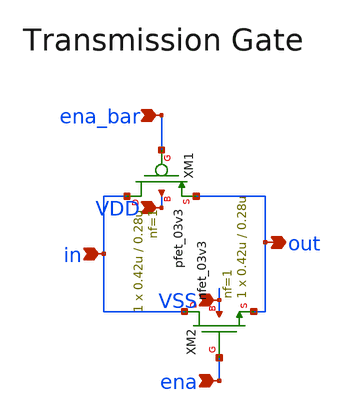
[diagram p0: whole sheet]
** sch_path: designs/libs/core_digital/schem/transmission_gate.sch
**.subckt transmission_gate in ena_bar ena VSS VDD out
*.ipin in
*.ipin ena_bar
*.ipin ena
*.ipin VSS
*.ipin VDD
*.opin out
XM1 in ena_bar out VDD pfet_03v3 L=0.28u W=0.42u nf=1 ad='int((nf+1)/2) * W/nf * 0.18u' as='int((nf+2)/2) * W/nf * 0.18u'
+ pd='2*int((nf+1)/2) * (W/nf + 0.18u)' ps='2*int((nf+2)/2) * (W/nf + 0.18u)' nrd='0.18u / W' nrs='0.18u / W'
+ sa=0 sb=0 sd=0 m=1
XM2 in ena out VSS nfet_03v3 L=0.28u W=0.42u nf=1 ad='int((nf+1)/2) * W/nf * 0.18u' as='int((nf+2)/2) * W/nf * 0.18u'
+ pd='2*int((nf+1)/2) * (W/nf + 0.18u)' ps='2*int((nf+2)/2) * (W/nf + 0.18u)' nrd='0.18u / W' nrs='0.18u / W'
+ sa=0 sb=0 sd=0 m=1
**.ends
.end
